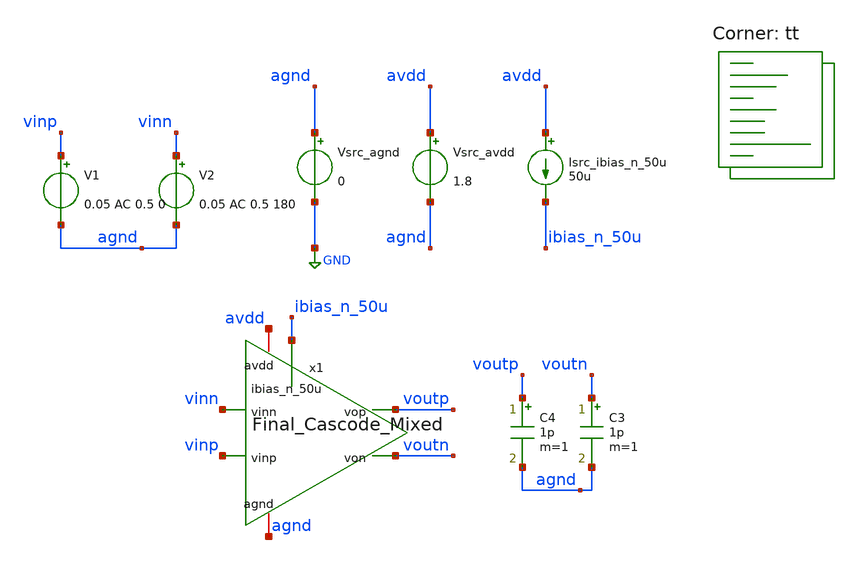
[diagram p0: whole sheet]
** sch_path: AMP/TB_Final_Cascode_Mixed.sch
**.subckt TB_Final_Cascode_Mixed
Vsrc_agnd agnd GND 0
Vsrc_avdd avdd agnd 1.8
Isrc_ibias_n_50u avdd ibias_n_50u 50u
C3 voutn agnd 1p m=1
C4 voutp agnd 1p m=1
V1 vinp agnd 0.05 AC 0.5 0
V2 vinn agnd 0.05 AC 0.5 180
x1 avdd voutp voutn vinn vinp ibias_n_50u agnd Final_Cascode_Mixed
**** begin user architecture code

* this option enables mos model bin
* selection based on W/NF instead of W
.option wnflag=1

.option savecurrents

.control
save all
op

* Print newline
echo

set nmos_list = ( x1.xm1 x1.xm2 x1.xm9 x1.xm10 )
set pmos_list = ( x1.xm7 x1.xm8 )
set nmos_lvt_list = ( x1.xm3 x1.xm4 )
set pmos_lvt_list = ( x1.xm5 x1.xm6 )

* Print stats for each MOSFET
foreach nmos $nmos_list
 * Save stats
 save @m.{$nmos}.msky130_fd_pr__nfet_01v8[gm]
 let vth   = @m.{$nmos}.msky130_fd_pr__nfet_01v8[vth]
 let vgs   = @m.{$nmos}.msky130_fd_pr__nfet_01v8[vgs]
 let vds   = @m.{$nmos}.msky130_fd_pr__nfet_01v8[vds]
 let vdsat = @m.{$nmos}.msky130_fd_pr__nfet_01v8[vdsat]
 let gm    = @m.{$nmos}.msky130_fd_pr__nfet_01v8[gm]
 let gds   = @m.{$nmos}.msky130_fd_pr__nfet_01v8[gds]


 * Print stats
 echo Stats for $nmos:
 print vth
 print vgs
 print vds
 print vdsat
 print gm
 print gds

 * Print newline
 echo
end

foreach pmos $pmos_list
 * Save stats
 save @m.{$pmos}.msky130_fd_pr__nfet_01v8[gm]
 let vth   = @m.{$pmos}.msky130_fd_pr__pfet_01v8[vth]
 let vgs   = @m.{$pmos}.msky130_fd_pr__pfet_01v8[vgs]
 let vds   = @m.{$pmos}.msky130_fd_pr__pfet_01v8[vds]
 let vdsat = @m.{$pmos}.msky130_fd_pr__pfet_01v8[vdsat]
 let gm    = @m.{$pmos}.msky130_fd_pr__pfet_01v8[gm]
 let gds   = @m.{$pmos}.msky130_fd_pr__pfet_01v8[gds]

 * Print stats
 echo Stats for $pmos:
 print vth
 print vgs
 print vds
 print vdsat
 print gm
 print gds

 * Print newline
 echo
end

foreach nmos_lvt $nmos_lvt_list
 * Save stats
 save @m.{$nmos_lvt}.msky130_fd_pr__nfet_01v8_lvt[gm]
 let vth   = @m.{$nmos_lvt}.msky130_fd_pr__nfet_01v8_lvt[vth]
 let vgs   = @m.{$nmos_lvt}.msky130_fd_pr__nfet_01v8_lvt[vgs]
 let vds   = @m.{$nmos_lvt}.msky130_fd_pr__nfet_01v8_lvt[vds]
 let vdsat = @m.{$nmos_lvt}.msky130_fd_pr__nfet_01v8_lvt[vdsat]
 let gm    = @m.{$nmos_lvt}.msky130_fd_pr__nfet_01v8_lvt[gm]
 let gds   = @m.{$nmos_lvt}.msky130_fd_pr__nfet_01v8_lvt[gds]


 * Print stats
 echo Stats for $nmos_lvt:
 print vth
 print vgs
 print vds
 print vdsat
 print gm
 print gds

 * Print newline
 echo
end

foreach pmos_lvt $pmos_lvt_list
 * Save stats
 save @m.{$pmos_lvt}.msky130_fd_pr__nfet_01v8_lvt[gm]
 let vth   = @m.{$pmos_lvt}.msky130_fd_pr__pfet_01v8_lvt[vth]
 let vgs   = @m.{$pmos_lvt}.msky130_fd_pr__pfet_01v8_lvt[vgs]
 let vds   = @m.{$pmos_lvt}.msky130_fd_pr__pfet_01v8_lvt[vds]
 let vdsat = @m.{$pmos_lvt}.msky130_fd_pr__pfet_01v8_lvt[vdsat]
 let gm    = @m.{$pmos_lvt}.msky130_fd_pr__pfet_01v8_lvt[gm]
 let gds   = @m.{$pmos_lvt}.msky130_fd_pr__pfet_01v8_lvt[gds]


 * Print stats
 echo Stats for $pmos_lvt:
 print vth
 print vgs
 print vds
 print vdsat
 print gm
 print gds

 * Print newline
 echo
end

* Print region of operation
echo Regions of Operation:
echo

echo NMOS:
foreach nmos $nmos_list
 * Save stats
 let vds = @m.{$nmos}.msky130_fd_pr__nfet_01v8[vds]
 let vgs = @m.{$nmos}.msky130_fd_pr__nfet_01v8[vgs]
 let vth = @m.{$nmos}.msky130_fd_pr__nfet_01v8[vth]

 * Check and print regions
 if (vgs <= vth)
  echo $nmos: N Cutoff
  print vgs
  print vth
 end
 if (vgs > vth) & (vds <= (vgs - vth))
  echo $nmos: N Triode
  print vgs
  print vth
  print vds
 end
 if (vgs > vth) & (vds > (vgs - vth))
  echo $nmos: N Saturation
 end
end
echo

echo PMOS:
foreach pmos $pmos_list
 * Save stats
 let vds = @m.{$pmos}.msky130_fd_pr__pfet_01v8[vds]
 let vgs = @m.{$pmos}.msky130_fd_pr__pfet_01v8[vgs]
 let vth = @m.{$pmos}.msky130_fd_pr__pfet_01v8[vth]

 * Check and print regions
 if (abs(vgs) <= abs(vth))
  echo $pmos: P Cutoff
  print vgs
  print vth
 end
 if (abs(vgs) > abs(vth)) & (abs(vds) <= (abs(vgs) - abs(vth)))
  echo $pmos: P Triode
  print vgs
  print vth
  print vds
 end
 if (abs(vgs) > abs(vth)) & (abs(vds) > (abs(vgs) - abs(vth)))
  echo $pmos: P Saturation
 end
end
echo

echo NMOS_lvt:
foreach nmos_lvt $nmos_lvt_list
 * Save stats
 let vds = @m.{$nmos_lvt}.msky130_fd_pr__nfet_01v8_lvt[vds]
 let vgs = @m.{$nmos_lvt}.msky130_fd_pr__nfet_01v8_lvt[vgs]
 let vth = @m.{$nmos_lvt}.msky130_fd_pr__nfet_01v8_lvt[vth]

 * Check and print regions
 if (vgs <= vth)
  echo $nmos_lvt: N Cutoff
  print vgs
  print vth
 end
 if (vgs > vth) & (vds <= (vgs - vth))
  echo $nmos_lvt: N Triode
  print vgs
  print vth
  print vds
 end
 if (vgs > vth) & (vds > (vgs - vth))
  echo $nmos_lvt: N Saturation
 end
end
echo

echo PMOS_lvt:
foreach pmos_lvt $pmos_lvt_list
 * Save stats
 let vds = @m.{$pmos_lvt}.msky130_fd_pr__pfet_01v8_lvt[vds]
 let vgs = @m.{$pmos_lvt}.msky130_fd_pr__pfet_01v8_lvt[vgs]
 let vth = @m.{$pmos_lvt}.msky130_fd_pr__pfet_01v8_lvt[vth]

 * Check and print regions
 if (abs(vgs) <= abs(vth))
  echo $pmos_lvt: P Cutoff
  print vgs
  print vth
 end
 if (abs(vgs) > abs(vth)) & (abs(vds) <= (abs(vgs) - abs(vth)))
  echo $pmos_lvt: P Triode
  print vgs
  print vth
  print vds
 end
 if (abs(vgs) > abs(vth)) & (abs(vds) > (abs(vgs) - abs(vth)))
  echo $pmos_lvt: P Saturation
 end
end
echo

* Sweep frequency
write TB_Final_Cascode_Mixed.raw
set appendwrite
ac dec 100 1 1e11
remzerovec

* Calculate gain
let vout_diff = v(voutp)- v(voutn)
let vin_diff = v(vinp)- v(vinn)
let gain = db(mag(vout_diff/vin_diff))
let ratio = (vout_diff/vin_diff)

write TB_Final_Cascode_Mixed.raw

.endc


.lib $::SKYWATER_MODELS/sky130.lib.spice tt
**** end user architecture code
**.ends

* expanding   symbol:
*+  /foss/designs/EE437/Project/ee437-quantum-controller/AMP/Final_Cascode_Mixed.sym # of pins=7
** sym_path: AMP/Final_Cascode_Mixed.sym
** sch_path: AMP/Final_Cascode_Mixed.sch
.subckt Final_Cascode_Mixed avdd vop von vinn vinp ibias_n_50u agnd
*.iopin avdd
*.ipin vinp
*.opin vop
*.iopin agnd
*.ipin vinn
*.opin von
*.ipin ibias_n_50u
Vsrc_Vb3_Ideal Vb3_Ideal agnd 0.81
Vsrc_Vb2_Ideal Vb2_Ideal agnd 0.59
Vsrc_Vb1_Ideal Vb1_Ideal agnd 1.52
Vsrc_Vb3 Vb3 Vb3_Ideal 0.0
Vsrc_Vb2 Vb2 Vb2_Ideal 0.0
Vsrc_Vb1 Vb1 Vb1_Ideal 0.0
Vsrc_vinp_cm_ideal1 vinp_cm_ideal vinp 1.35
Vsrc_vinp_cm_ideal vinn_cm_ideal vinn 1.35
Vsrc_vinn_cm vinn_cm vinn_cm_ideal 0.0
Vsrc_vinp_cm vinp_cm vinp_cm_ideal 0.0
XM1 int_n1 vinp_cm itail agnd sky130_fd_pr__nfet_01v8 L=0.15 W=0.97 nf=1 ad='int((nf+1)/2) * W/nf * 0.29'
+ as='int((nf+2)/2) * W/nf * 0.29' pd='2*int((nf+1)/2) * (W/nf + 0.29)' ps='2*int((nf+2)/2) * (W/nf + 0.29)'
+ nrd='0.29 / W' nrs='0.29 / W' sa=0 sb=0 sd=0 mult=1 m=1
XM2 int_n2 vinn_cm itail agnd sky130_fd_pr__nfet_01v8 L=0.15 W=0.97 nf=1 ad='int((nf+1)/2) * W/nf * 0.29'
+ as='int((nf+2)/2) * W/nf * 0.29' pd='2*int((nf+1)/2) * (W/nf + 0.29)' ps='2*int((nf+2)/2) * (W/nf + 0.29)'
+ nrd='0.29 / W' nrs='0.29 / W' sa=0 sb=0 sd=0 mult=1 m=1
XM7 int_p1 Vb3 avdd avdd sky130_fd_pr__pfet_01v8 L=0.35 W=2.20 nf=1 ad='int((nf+1)/2) * W/nf * 0.29'
+ as='int((nf+2)/2) * W/nf * 0.29' pd='2*int((nf+1)/2) * (W/nf + 0.29)' ps='2*int((nf+2)/2) * (W/nf + 0.29)'
+ nrd='0.29 / W' nrs='0.29 / W' sa=0 sb=0 sd=0 mult=4 m=4
XM8 int_p2 Vb3 avdd avdd sky130_fd_pr__pfet_01v8 L=0.35 W=2.20 nf=1 ad='int((nf+1)/2) * W/nf * 0.29'
+ as='int((nf+2)/2) * W/nf * 0.29' pd='2*int((nf+1)/2) * (W/nf + 0.29)' ps='2*int((nf+2)/2) * (W/nf + 0.29)'
+ nrd='0.29 / W' nrs='0.29 / W' sa=0 sb=0 sd=0 mult=4 m=4
XM9 ibias_n_50u ibias_n_50u agnd agnd sky130_fd_pr__nfet_01v8 L=0.15 W=1.15 nf=1 ad='int((nf+1)/2) * W/nf * 0.29'
+ as='int((nf+2)/2) * W/nf * 0.29' pd='2*int((nf+1)/2) * (W/nf + 0.29)' ps='2*int((nf+2)/2) * (W/nf + 0.29)'
+ nrd='0.29 / W' nrs='0.29 / W' sa=0 sb=0 sd=0 mult=2 m=2
XM10 itail ibias_n_50u agnd agnd sky130_fd_pr__nfet_01v8 L=0.15 W=1.15 nf=1 ad='int((nf+1)/2) * W/nf * 0.29'
+ as='int((nf+2)/2) * W/nf * 0.29' pd='2*int((nf+1)/2) * (W/nf + 0.29)' ps='2*int((nf+2)/2) * (W/nf + 0.29)'
+ nrd='0.29 / W' nrs='0.29 / W' sa=0 sb=0 sd=0 mult=16 m=16
XM3 von Vb1 int_n1 agnd sky130_fd_pr__nfet_01v8_lvt L=0.15 W=1.16 nf=1 ad='int((nf+1)/2) * W/nf * 0.29'
+ as='int((nf+2)/2) * W/nf * 0.29' pd='2*int((nf+1)/2) * (W/nf + 0.29)' ps='2*int((nf+2)/2) * (W/nf + 0.29)'
+ nrd='0.29 / W' nrs='0.29 / W' sa=0 sb=0 sd=0 mult=8 m=8
XM4 vop Vb1 int_n2 agnd sky130_fd_pr__nfet_01v8_lvt L=0.15 W=1.16 nf=1 ad='int((nf+1)/2) * W/nf * 0.29'
+ as='int((nf+2)/2) * W/nf * 0.29' pd='2*int((nf+1)/2) * (W/nf + 0.29)' ps='2*int((nf+2)/2) * (W/nf + 0.29)'
+ nrd='0.29 / W' nrs='0.29 / W' sa=0 sb=0 sd=0 mult=8 m=8
XM5 von Vb2 int_p1 avdd sky130_fd_pr__pfet_01v8_lvt L=0.35 W=1.32 nf=1 ad='int((nf+1)/2) * W/nf * 0.29'
+ as='int((nf+2)/2) * W/nf * 0.29' pd='2*int((nf+1)/2) * (W/nf + 0.29)' ps='2*int((nf+2)/2) * (W/nf + 0.29)'
+ nrd='0.29 / W' nrs='0.29 / W' sa=0 sb=0 sd=0 mult=32 m=32
XM6 vop Vb2 int_p2 avdd sky130_fd_pr__pfet_01v8_lvt L=0.35 W=1.32 nf=1 ad='int((nf+1)/2) * W/nf * 0.29'
+ as='int((nf+2)/2) * W/nf * 0.29' pd='2*int((nf+1)/2) * (W/nf + 0.29)' ps='2*int((nf+2)/2) * (W/nf + 0.29)'
+ nrd='0.29 / W' nrs='0.29 / W' sa=0 sb=0 sd=0 mult=32 m=32
I0 itail_ideal net1 400u
V1 net1 agnd 0.3
.ends

.GLOBAL GND
.end
